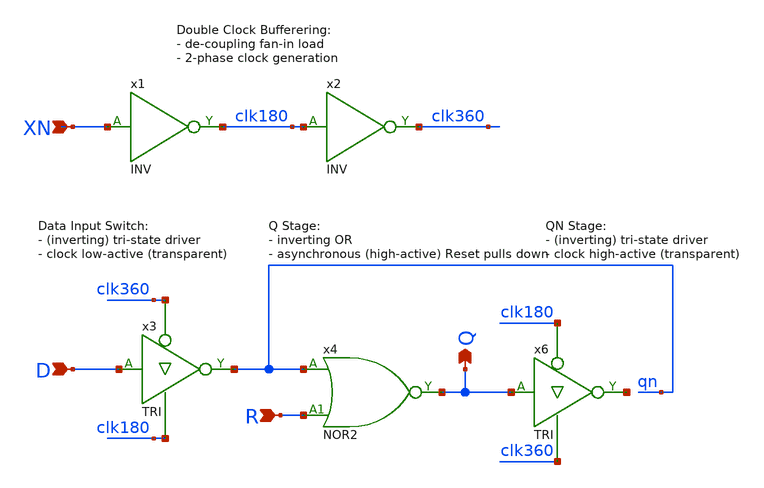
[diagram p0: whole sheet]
** sch_path: Sources/crafted/LATNR.sch
**.subckt LATNR XN D Q R
*.ipin XN
*.ipin D
*.opin Q
*.ipin R
x4 qn R Q VDD GND NOR2 Wmin=1.5u Lmin=1u g=2 m=1
x2 clk180 clk360 VDD GND INV Wmin=1.5u Lmin=1u g=2 m=1
x1 XN clk180 VDD GND INV Wmin=1.5u Lmin=1u g=2 m=1
x3 D clk360 clk180 qn VDD GND TRI Wmin=1.5u Lmin=1u g=2 m=1
x6 Q clk180 clk360 net1 VDD GND TRI Wmin=1.5u Lmin=1u g=2 m=1
**.ends
.end
